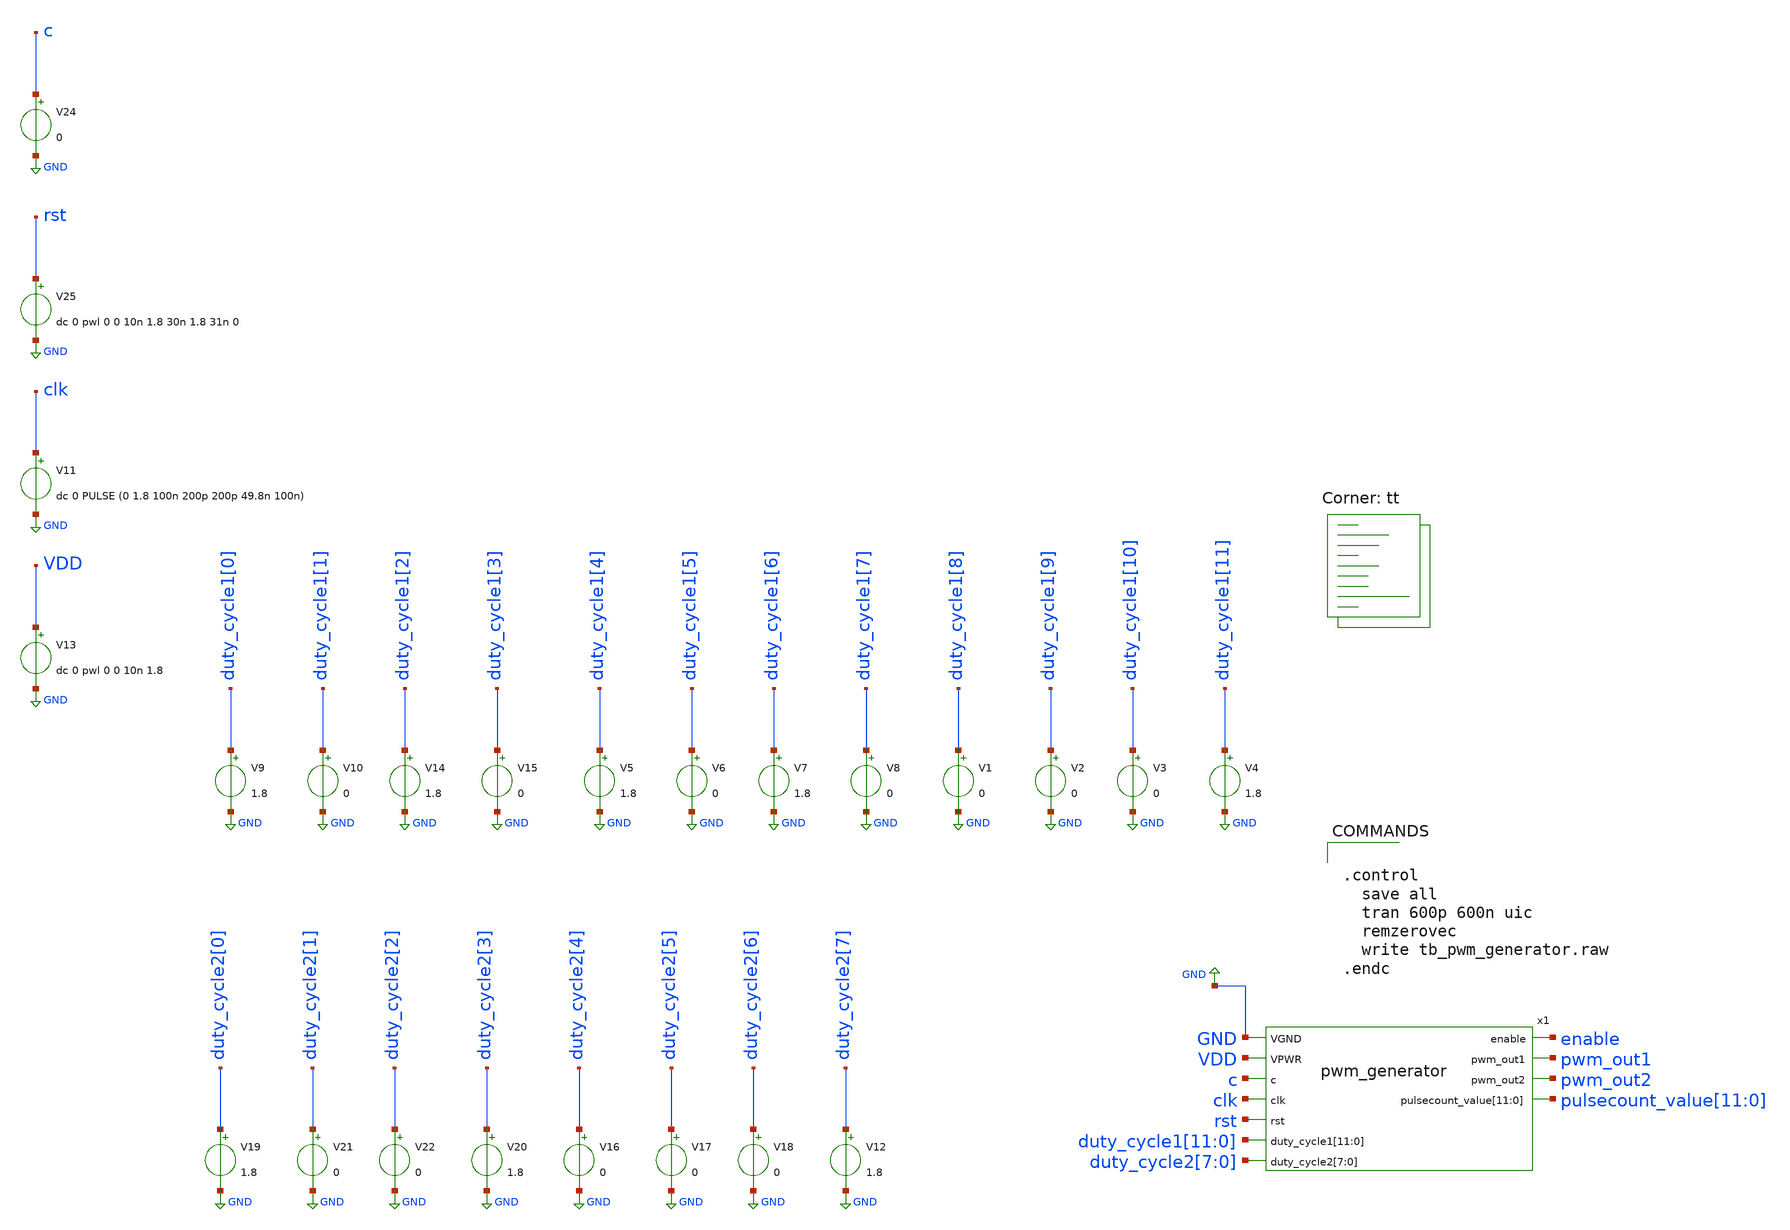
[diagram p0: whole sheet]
** sch_path: xschem/tb_pwm_generator.sch
**.subckt tb_pwm_generator
x1 enable GND pwm_out1 VDD pwm_out2 c pulsecount_value[11] pulsecount_value[10] pulsecount_value[9]
+ pulsecount_value[8] pulsecount_value[7] pulsecount_value[6] pulsecount_value[5] pulsecount_value[4] pulsecount_value[3]
+ pulsecount_value[2] pulsecount_value[1] pulsecount_value[0] clk rst duty_cycle1[11] duty_cycle1[10] duty_cycle1[9]
+ duty_cycle1[8] duty_cycle1[7] duty_cycle1[6] duty_cycle1[5] duty_cycle1[4] duty_cycle1[3] duty_cycle1[2]
+ duty_cycle1[1] duty_cycle1[0] duty_cycle2[7] duty_cycle2[6] duty_cycle2[5] duty_cycle2[4] duty_cycle2[3]
+ duty_cycle2[2] duty_cycle2[1] duty_cycle2[0] pwm_generator
V1 duty_cycle1[8] GND 0
V2 duty_cycle1[9] GND 0
V3 duty_cycle1[10] GND 0
V4 duty_cycle1[11] GND 1.8
V5 duty_cycle1[4] GND 1.8
V6 duty_cycle1[5] GND 0
V7 duty_cycle1[6] GND 1.8
V8 duty_cycle1[7] GND 0
V9 duty_cycle1[0] GND 1.8
V10 duty_cycle1[1] GND 0
V14 duty_cycle1[2] GND 1.8
V15 duty_cycle1[3] GND 0
V16 duty_cycle2[4] GND 0
V17 duty_cycle2[5] GND 0
V18 duty_cycle2[6] GND 0
V12 duty_cycle2[7] GND 1.8
V19 duty_cycle2[0] GND 1.8
V21 duty_cycle2[1] GND 0
V22 duty_cycle2[2] GND 0
V20 duty_cycle2[3] GND 1.8
V11 clk GND dc 0 PULSE (0 1.8 100n 200p 200p 49.8n 100n)
V13 VDD GND dc 0 pwl 0 0 10n 1.8
V24 c GND 0
V25 rst GND dc 0 pwl 0 0 10n 1.8 30n 1.8 31n 0
**** begin user architecture code


.control
  save all
  tran 600p 600n uic
  remzerovec
  write tb_pwm_generator.raw
.endc



** opencircuitdesign pdks install
.include $::SKYWATER_STDCELLS/sky130_fd_sc_hd.spice


.lib $::SKYWATER_MODELS/sky130.lib.spice tt
**** end user architecture code
**.ends

* expanding   symbol:  pwm_generator.sym # of pins=11
** sym_path: xschem/pwm_generator.sym
** sch_path: xschem/pwm_generator.sch
.subckt pwm_generator enable VGND pwm_out1 VPWR pwm_out2 c pulsecount_value[11] pulsecount_value[10]
+ pulsecount_value[9] pulsecount_value[8] pulsecount_value[7] pulsecount_value[6] pulsecount_value[5] pulsecount_value[4]
+ pulsecount_value[3] pulsecount_value[2] pulsecount_value[1] pulsecount_value[0] clk rst duty_cycle1[11] duty_cycle1[10]
+ duty_cycle1[9] duty_cycle1[8] duty_cycle1[7] duty_cycle1[6] duty_cycle1[5] duty_cycle1[4] duty_cycle1[3]
+ duty_cycle1[2] duty_cycle1[1] duty_cycle1[0] duty_cycle2[7] duty_cycle2[6] duty_cycle2[5] duty_cycle2[4]
+ duty_cycle2[3] duty_cycle2[2] duty_cycle2[1] duty_cycle2[0]
*.ipin VGND
*.ipin VPWR
*.ipin c
*.ipin clk
*.opin enable
*.opin pwm_out1
*.opin pwm_out2
*.ipin rst
*.ipin
*+ duty_cycle1[11],duty_cycle1[10],duty_cycle1[9],duty_cycle1[8],duty_cycle1[7],duty_cycle1[6],duty_cycle1[5],duty_cycle1[4],duty_cycle1[3],duty_cycle1[2],duty_cycle1[1],duty_cycle1[0]
*.ipin
*+ duty_cycle2[7],duty_cycle2[6],duty_cycle2[5],duty_cycle2[4],duty_cycle2[3],duty_cycle2[2],duty_cycle2[1],duty_cycle2[0]
*.opin
*+ pulsecount_value[11],pulsecount_value[10],pulsecount_value[9],pulsecount_value[8],pulsecount_value[7],pulsecount_value[6],pulsecount_value[5],pulsecount_value[4],pulsecount_value[3],pulsecount_value[2],pulsecount_value[1],pulsecount_value[0]
X_274_ prev_pwm_out1 net36 pulse__counter_o0_c pulse__counter_o1_c VGND VGND VPWR VPWR _084_
+ sky130_fd_sc_hd__and4b_1
X_275_ pulse__counter_o3_c pulse__counter_o2_c _084_ VGND VGND VPWR VPWR _085_
+ sky130_fd_sc_hd__and3_1
X_276_ pulse__counter_o5_c pulse__counter_o4_c _085_ VGND VGND VPWR VPWR _086_
+ sky130_fd_sc_hd__and3_1
X_277_ pulse__counter_o8_c pulse__counter_o7_c pulse__counter_o6_c _086_ VGND VGND VPWR VPWR _087_
+ sky130_fd_sc_hd__and4_1
X_278_ pulse__counter_o10_c pulse__counter_o9_c _087_ VGND VGND VPWR VPWR _088_
+ sky130_fd_sc_hd__and3_1
X_279_ net39 _088_ VGND VGND VPWR VPWR _083_ sky130_fd_sc_hd__xor2_1
X_280_ net67 _087_ net52 VGND VGND VPWR VPWR _089_ sky130_fd_sc_hd__a21oi_1
X_281_ _088_ _089_ VGND VGND VPWR VPWR _082_ sky130_fd_sc_hd__nor2_1
X_282_ net54 _087_ VGND VGND VPWR VPWR _081_ sky130_fd_sc_hd__xor2_1
X_283_ pulse__counter_o7_c pulse__counter_o6_c _086_ pulse__counter_o8_c VGND VGND VPWR VPWR _090_
+ sky130_fd_sc_hd__a31o_1
X_284_ _087_ _090_ VGND VGND VPWR VPWR _091_ sky130_fd_sc_hd__and2b_1
X_285_ _091_ VGND VGND VPWR VPWR _080_ sky130_fd_sc_hd__clkbuf_1
X_286_ pulse__counter_o6_c _086_ VGND VGND VPWR VPWR _092_ sky130_fd_sc_hd__nand2_1
X_287_ net49 _092_ VGND VGND VPWR VPWR _079_ sky130_fd_sc_hd__xnor2_1
X_288_ pulse__counter_o6_c _086_ VGND VGND VPWR VPWR _093_ sky130_fd_sc_hd__or2_1
X_289_ _092_ _093_ VGND VGND VPWR VPWR _094_ sky130_fd_sc_hd__and2_1
X_290_ _094_ VGND VGND VPWR VPWR _078_ sky130_fd_sc_hd__clkbuf_1
X_291_ pulse__counter_o4_c _085_ pulse__counter_o5_c VGND VGND VPWR VPWR _095_
+ sky130_fd_sc_hd__a21o_1
X_292_ _086_ _095_ VGND VGND VPWR VPWR _096_ sky130_fd_sc_hd__and2b_1
X_293_ _096_ VGND VGND VPWR VPWR _077_ sky130_fd_sc_hd__clkbuf_1
X_294_ net41 _085_ VGND VGND VPWR VPWR _076_ sky130_fd_sc_hd__xor2_1
X_295_ net66 _084_ net42 VGND VGND VPWR VPWR _097_ sky130_fd_sc_hd__a21oi_1
X_296_ _085_ _097_ VGND VGND VPWR VPWR _075_ sky130_fd_sc_hd__nor2_1
X_297_ net47 _084_ VGND VGND VPWR VPWR _074_ sky130_fd_sc_hd__xor2_1
X_298_ prev_pwm_out1 VGND VGND VPWR VPWR _098_ sky130_fd_sc_hd__inv_2
X_299_ pulse__counter_o0_c net36 _098_ VGND VGND VPWR VPWR _099_ sky130_fd_sc_hd__and3_1
X_300_ net59 _099_ _084_ VGND VGND VPWR VPWR _073_ sky130_fd_sc_hd__o21ba_1
X_301_ net36 _098_ net61 VGND VGND VPWR VPWR _100_ sky130_fd_sc_hd__a21oi_1
X_302_ _099_ net62 VGND VGND VPWR VPWR _072_ sky130_fd_sc_hd__nor2_1
X_303_ net20 VGND VGND VPWR VPWR _101_ sky130_fd_sc_hd__inv_2
X_304_ counter2_o7_c _101_ VGND VGND VPWR VPWR _102_ sky130_fd_sc_hd__nand2_1
X_305_ counter2_o6_c VGND VGND VPWR VPWR _103_ sky130_fd_sc_hd__inv_2
X_306_ counter2_o3_c VGND VGND VPWR VPWR _104_ sky130_fd_sc_hd__inv_2
X_307_ net15 counter2_o2_c VGND VGND VPWR VPWR _105_ sky130_fd_sc_hd__or2b_1
X_308_ counter2_o1_c net14 VGND VGND VPWR VPWR _106_ sky130_fd_sc_hd__and2b_1
X_309_ counter2_o2_c net15 VGND VGND VPWR VPWR _107_ sky130_fd_sc_hd__and2b_1
X_310_ _104_ net16 _105_ _106_ _107_ VGND VGND VPWR VPWR _108_ sky130_fd_sc_hd__a221o_1
X_311_ counter2_o4_c VGND VGND VPWR VPWR _109_ sky130_fd_sc_hd__inv_2
X_312_ _109_ net17 net16 _104_ VGND VGND VPWR VPWR _110_ sky130_fd_sc_hd__o22a_1
X_313_ counter2_o5_c VGND VGND VPWR VPWR _111_ sky130_fd_sc_hd__inv_2
X_314_ _109_ net17 net18 _111_ VGND VGND VPWR VPWR _112_ sky130_fd_sc_hd__a22o_1
X_315_ _108_ _110_ _112_ VGND VGND VPWR VPWR _113_ sky130_fd_sc_hd__a21o_1
X_316_ _103_ net19 net18 _111_ VGND VGND VPWR VPWR _114_ sky130_fd_sc_hd__o22a_1
X_317_ _103_ net19 _113_ _114_ VGND VGND VPWR VPWR _115_ sky130_fd_sc_hd__a22o_1
X_318_ counter2_o7_c _101_ VGND VGND VPWR VPWR _116_ sky130_fd_sc_hd__nor2_1
X_319_ _102_ _115_ _116_ net21 VGND VGND VPWR VPWR _117_ sky130_fd_sc_hd__a211o_2
X_320_ counter2_o3_c counter2_o2_c counter2_o1_c counter2_o0_c VGND VGND VPWR VPWR _118_
+ sky130_fd_sc_hd__and4_1
X_321_ counter2_o4_c _118_ VGND VGND VPWR VPWR _119_ sky130_fd_sc_hd__nand2_1
X_322_ _111_ _119_ VGND VGND VPWR VPWR _120_ sky130_fd_sc_hd__nor2_1
X_323_ counter2_o6_c _120_ VGND VGND VPWR VPWR _121_ sky130_fd_sc_hd__nand2_1
X_324_ counter2_o7_c _121_ VGND VGND VPWR VPWR _122_ sky130_fd_sc_hd__xnor2_1
X_325_ _117_ _122_ VGND VGND VPWR VPWR _123_ sky130_fd_sc_hd__and2_1
X_326_ _123_ VGND VGND VPWR VPWR _071_ sky130_fd_sc_hd__clkbuf_1
X_327_ counter2_o6_c _120_ VGND VGND VPWR VPWR _124_ sky130_fd_sc_hd__or2_1
X_328_ _117_ _121_ _124_ VGND VGND VPWR VPWR _125_ sky130_fd_sc_hd__and3_1
X_329_ _125_ VGND VGND VPWR VPWR _070_ sky130_fd_sc_hd__clkbuf_1
X_330_ _120_ VGND VGND VPWR VPWR _126_ sky130_fd_sc_hd__inv_2
X_331_ _111_ _119_ VGND VGND VPWR VPWR _127_ sky130_fd_sc_hd__nand2_1
X_332_ _117_ _126_ _127_ VGND VGND VPWR VPWR _128_ sky130_fd_sc_hd__and3_1
X_333_ _128_ VGND VGND VPWR VPWR _069_ sky130_fd_sc_hd__clkbuf_1
X_334_ counter2_o4_c _118_ VGND VGND VPWR VPWR _129_ sky130_fd_sc_hd__or2_1
X_335_ _117_ _119_ _129_ VGND VGND VPWR VPWR _130_ sky130_fd_sc_hd__and3_1
X_336_ _130_ VGND VGND VPWR VPWR _068_ sky130_fd_sc_hd__clkbuf_1
X_337_ _118_ VGND VGND VPWR VPWR _131_ sky130_fd_sc_hd__inv_2
X_338_ counter2_o2_c counter2_o1_c counter2_o0_c VGND VGND VPWR VPWR _132_ sky130_fd_sc_hd__nand3_1
X_339_ _104_ _132_ VGND VGND VPWR VPWR _133_ sky130_fd_sc_hd__nand2_1
X_340_ _117_ _131_ _133_ VGND VGND VPWR VPWR _134_ sky130_fd_sc_hd__and3_1
X_341_ _134_ VGND VGND VPWR VPWR _067_ sky130_fd_sc_hd__clkbuf_1
X_342_ counter2_o1_c counter2_o0_c counter2_o2_c VGND VGND VPWR VPWR _135_ sky130_fd_sc_hd__a21o_1
X_343_ _117_ _132_ _135_ VGND VGND VPWR VPWR _136_ sky130_fd_sc_hd__and3_1
X_344_ _136_ VGND VGND VPWR VPWR _066_ sky130_fd_sc_hd__clkbuf_1
X_345_ counter2_o1_c counter2_o0_c VGND VGND VPWR VPWR _137_ sky130_fd_sc_hd__nand2_1
X_346_ counter2_o1_c counter2_o0_c VGND VGND VPWR VPWR _138_ sky130_fd_sc_hd__or2_1
X_347_ _117_ _137_ _138_ VGND VGND VPWR VPWR _139_ sky130_fd_sc_hd__and3_1
X_348_ _139_ VGND VGND VPWR VPWR _065_ sky130_fd_sc_hd__clkbuf_1
X_349_ counter2_o0_c _117_ VGND VGND VPWR VPWR _140_ sky130_fd_sc_hd__and2b_1
X_350_ _140_ VGND VGND VPWR VPWR _064_ sky130_fd_sc_hd__clkbuf_1
X_351_ counter1_o11_c VGND VGND VPWR VPWR _141_ sky130_fd_sc_hd__inv_2
X_352_ _141_ net3 net4 VGND VGND VPWR VPWR _142_ sky130_fd_sc_hd__a21oi_2
X_353_ _142_ VGND VGND VPWR VPWR _143_ sky130_fd_sc_hd__buf_2
X_354_ net13 VGND VGND VPWR VPWR _144_ sky130_fd_sc_hd__inv_2
X_355_ counter1_o10_c _144_ VGND VGND VPWR VPWR _145_ sky130_fd_sc_hd__or2_1
X_356_ counter1_o9_c net12 VGND VGND VPWR VPWR _146_ sky130_fd_sc_hd__xnor2_1
X_357_ net11 counter1_o8_c VGND VGND VPWR VPWR _147_ sky130_fd_sc_hd__or2b_1
X_358_ net10 counter1_o7_c VGND VGND VPWR VPWR _148_ sky130_fd_sc_hd__or2b_1
X_359_ _147_ _148_ VGND VGND VPWR VPWR _149_ sky130_fd_sc_hd__nand2_1
X_360_ counter1_o8_c net11 VGND VGND VPWR VPWR _150_ sky130_fd_sc_hd__or2b_1
X_361_ net9 VGND VGND VPWR VPWR _151_ sky130_fd_sc_hd__inv_2
X_362_ net8 VGND VGND VPWR VPWR _152_ sky130_fd_sc_hd__inv_2
X_363_ counter1_o6_c _151_ _152_ counter1_o5_c VGND VGND VPWR VPWR _153_ sky130_fd_sc_hd__a22o_1
X_364_ counter1_o4_c VGND VGND VPWR VPWR _154_ sky130_fd_sc_hd__inv_2
X_365_ _154_ net7 VGND VGND VPWR VPWR _155_ sky130_fd_sc_hd__nand2_1
X_366_ counter1_o7_c net10 VGND VGND VPWR VPWR _156_ sky130_fd_sc_hd__or2b_1
X_367_ _147_ _148_ _156_ _150_ VGND VGND VPWR VPWR _157_ sky130_fd_sc_hd__and4_1
X_368_ counter1_o6_c _151_ _152_ counter1_o5_c VGND VGND VPWR VPWR _158_ sky130_fd_sc_hd__o22a_1
X_369_ _153_ _155_ _157_ _158_ VGND VGND VPWR VPWR _159_ sky130_fd_sc_hd__and4b_1
X_370_ net6 VGND VGND VPWR VPWR _160_ sky130_fd_sc_hd__inv_2
X_371_ net5 VGND VGND VPWR VPWR _161_ sky130_fd_sc_hd__inv_2
X_372_ net2 VGND VGND VPWR VPWR _162_ sky130_fd_sc_hd__inv_2
X_373_ counter1_o2_c _161_ _162_ counter1_o1_c VGND VGND VPWR VPWR _163_ sky130_fd_sc_hd__a211o_1
X_374_ counter1_o2_c _161_ _160_ counter1_o3_c VGND VGND VPWR VPWR _164_ sky130_fd_sc_hd__o22a_1
X_375_ _154_ net7 VGND VGND VPWR VPWR _165_ sky130_fd_sc_hd__nor2_1
X_376_ counter1_o3_c _160_ _163_ _164_ _165_ VGND VGND VPWR VPWR _166_ sky130_fd_sc_hd__a221o_1
X_377_ counter1_o6_c _151_ _153_ _157_ VGND VGND VPWR VPWR _167_ sky130_fd_sc_hd__o211a_1
X_378_ _149_ _150_ _159_ _166_ _167_ VGND VGND VPWR VPWR _168_ sky130_fd_sc_hd__a221o_1
X_379_ net3 VGND VGND VPWR VPWR _169_ sky130_fd_sc_hd__inv_2
X_380_ net12 _145_ counter1_o9_c VGND VGND VPWR VPWR _170_ sky130_fd_sc_hd__and3b_1
X_381_ counter1_o11_c _169_ _144_ counter1_o10_c _170_ VGND VGND VPWR VPWR _171_
+ sky130_fd_sc_hd__a221o_1
X_382_ _145_ _146_ _168_ _171_ VGND VGND VPWR VPWR _172_ sky130_fd_sc_hd__a31o_1
X_383_ _172_ VGND VGND VPWR VPWR _173_ sky130_fd_sc_hd__buf_2
X_384_ counter1_o3_c counter1_o2_c counter1_o1_c counter1_o0_c VGND VGND VPWR VPWR _174_
+ sky130_fd_sc_hd__and4_1
X_385_ _174_ VGND VGND VPWR VPWR _175_ sky130_fd_sc_hd__dlymetal6s2s_1
X_386_ counter1_o5_c counter1_o4_c VGND VGND VPWR VPWR _176_ sky130_fd_sc_hd__and2_1
X_387_ counter1_o7_c counter1_o6_c _175_ _176_ VGND VGND VPWR VPWR _177_ sky130_fd_sc_hd__and4_1
X_388_ counter1_o9_c counter1_o8_c _177_ VGND VGND VPWR VPWR _178_ sky130_fd_sc_hd__and3_1
X_389_ counter1_o10_c _178_ VGND VGND VPWR VPWR _179_ sky130_fd_sc_hd__and2_1
X_390_ net64 _179_ VGND VGND VPWR VPWR _180_ sky130_fd_sc_hd__xnor2_1
X_391_ _143_ _173_ _180_ VGND VGND VPWR VPWR _063_ sky130_fd_sc_hd__a21oi_1
X_392_ counter1_o10_c _178_ VGND VGND VPWR VPWR _181_ sky130_fd_sc_hd__nor2_1
X_393_ _143_ _173_ _179_ _181_ VGND VGND VPWR VPWR _062_ sky130_fd_sc_hd__a211oi_1
X_394_ counter1_o8_c _177_ counter1_o9_c VGND VGND VPWR VPWR _182_ sky130_fd_sc_hd__a21oi_1
X_395_ _143_ _173_ _178_ _182_ VGND VGND VPWR VPWR _061_ sky130_fd_sc_hd__a211oi_1
X_396_ counter1_o8_c _177_ VGND VGND VPWR VPWR _183_ sky130_fd_sc_hd__xnor2_1
X_397_ _143_ _173_ _183_ VGND VGND VPWR VPWR _060_ sky130_fd_sc_hd__a21oi_1
X_398_ _175_ _176_ VGND VGND VPWR VPWR _184_ sky130_fd_sc_hd__and2_1
X_399_ counter1_o6_c _184_ counter1_o7_c VGND VGND VPWR VPWR _185_ sky130_fd_sc_hd__a21oi_1
X_400_ _143_ _173_ _177_ _185_ VGND VGND VPWR VPWR _059_ sky130_fd_sc_hd__a211oi_1
X_401_ counter1_o6_c _184_ VGND VGND VPWR VPWR _186_ sky130_fd_sc_hd__xnor2_1
X_402_ _143_ _173_ _186_ VGND VGND VPWR VPWR _058_ sky130_fd_sc_hd__a21oi_1
X_403_ counter1_o4_c _175_ counter1_o5_c VGND VGND VPWR VPWR _187_ sky130_fd_sc_hd__a21oi_1
X_404_ _142_ _172_ _184_ _187_ VGND VGND VPWR VPWR _057_ sky130_fd_sc_hd__a211oi_1
X_405_ counter1_o4_c _175_ VGND VGND VPWR VPWR _188_ sky130_fd_sc_hd__xnor2_1
X_406_ _143_ _173_ _188_ VGND VGND VPWR VPWR _056_ sky130_fd_sc_hd__a21oi_1
X_407_ counter1_o2_c counter1_o1_c counter1_o0_c VGND VGND VPWR VPWR _189_ sky130_fd_sc_hd__and3_1
X_408_ counter1_o3_c _189_ VGND VGND VPWR VPWR _190_ sky130_fd_sc_hd__nor2_1
X_409_ _142_ _172_ _175_ _190_ VGND VGND VPWR VPWR _055_ sky130_fd_sc_hd__a211oi_1
X_410_ counter1_o1_c counter1_o0_c counter1_o2_c VGND VGND VPWR VPWR _191_ sky130_fd_sc_hd__a21oi_1
X_411_ _142_ _172_ _189_ _191_ VGND VGND VPWR VPWR _054_ sky130_fd_sc_hd__a211oi_1
X_412_ net65 net40 VGND VGND VPWR VPWR _192_ sky130_fd_sc_hd__xnor2_1
X_413_ _143_ _173_ _192_ VGND VGND VPWR VPWR _053_ sky130_fd_sc_hd__a21oi_1
X_414_ _143_ _173_ net40 VGND VGND VPWR VPWR _052_ sky130_fd_sc_hd__a21oi_1
X_415_ pulse__counter_o11_c pulse__counter_o10_c pulse__counter_o9_c pulse__counter_o8_c VGND VGND
+ VPWR VPWR _193_ sky130_fd_sc_hd__nor4_1
X_416_ pulse__counter_o3_c pulse__counter_o2_c pulse__counter_o1_c pulse__counter_o0_c VGND VGND
+ VPWR VPWR _194_ sky130_fd_sc_hd__and4b_1
X_417_ pulse__counter_o7_c pulse__counter_o6_c pulse__counter_o5_c pulse__counter_o4_c VGND VGND
+ VPWR VPWR _195_ sky130_fd_sc_hd__nor4_1
X_418_ _193_ _194_ _195_ net38 VGND VGND VPWR VPWR _039_ sky130_fd_sc_hd__a31o_1
X_419_ net21 counter2_o7_c VGND VGND VPWR VPWR _196_ sky130_fd_sc_hd__and2b_1
X_420_ _109_ net18 VGND VGND VPWR VPWR _197_ sky130_fd_sc_hd__or2_1
X_421_ counter2_o0_c net14 VGND VGND VPWR VPWR _198_ sky130_fd_sc_hd__and2b_1
X_422_ counter2_o1_c net15 VGND VGND VPWR VPWR _199_ sky130_fd_sc_hd__and2b_1
X_423_ net15 counter2_o1_c VGND VGND VPWR VPWR _200_ sky130_fd_sc_hd__and2b_1
X_424_ net14 counter2_o0_c VGND VGND VPWR VPWR _201_ sky130_fd_sc_hd__and2b_1
X_425_ _199_ _200_ _201_ VGND VGND VPWR VPWR _202_ sky130_fd_sc_hd__or3_1
X_426_ counter2_o3_c net17 VGND VGND VPWR VPWR _203_ sky130_fd_sc_hd__or2b_1
X_427_ net17 counter2_o3_c VGND VGND VPWR VPWR _204_ sky130_fd_sc_hd__or2b_1
X_428_ counter2_o2_c net16 VGND VGND VPWR VPWR _205_ sky130_fd_sc_hd__or2b_1
X_429_ net16 counter2_o2_c VGND VGND VPWR VPWR _206_ sky130_fd_sc_hd__or2b_1
X_430_ _203_ _204_ _205_ _206_ VGND VGND VPWR VPWR _207_ sky130_fd_sc_hd__and4_1
X_431_ _198_ _202_ _207_ VGND VGND VPWR VPWR _208_ sky130_fd_sc_hd__or3b_1
X_432_ _200_ _201_ _199_ VGND VGND VPWR VPWR _209_ sky130_fd_sc_hd__o21bai_1
X_433_ counter2_o2_c net16 _204_ VGND VGND VPWR VPWR _210_ sky130_fd_sc_hd__and3b_1
X_434_ _104_ net17 _207_ _209_ _210_ VGND VGND VPWR VPWR _211_ sky130_fd_sc_hd__a221o_1
X_435_ _111_ net19 net18 _109_ VGND VGND VPWR VPWR _212_ sky130_fd_sc_hd__a22o_1
X_436_ _197_ _208_ _211_ _212_ VGND VGND VPWR VPWR _213_ sky130_fd_sc_hd__a31oi_1
X_437_ net19 _111_ counter2_o6_c _101_ VGND VGND VPWR VPWR _214_ sky130_fd_sc_hd__a2bb2o_1
X_438_ counter2_o7_c net21 VGND VGND VPWR VPWR _215_ sky130_fd_sc_hd__or2b_1
X_439_ counter2_o6_c _101_ _213_ _214_ _215_ VGND VGND VPWR VPWR _216_ sky130_fd_sc_hd__o221a_1
X_440_ _196_ _216_ _117_ VGND VGND VPWR VPWR _038_ sky130_fd_sc_hd__o21ai_1
X_441_ counter1_o8_c VGND VGND VPWR VPWR _217_ sky130_fd_sc_hd__inv_2
X_442_ _141_ net4 _169_ counter1_o10_c VGND VGND VPWR VPWR _218_ sky130_fd_sc_hd__a22o_1
X_443_ _141_ net4 VGND VGND VPWR VPWR _219_ sky130_fd_sc_hd__or2_1
X_444_ counter1_o9_c VGND VGND VPWR VPWR _220_ sky130_fd_sc_hd__inv_2
X_445_ counter1_o10_c _169_ net13 _220_ VGND VGND VPWR VPWR _221_ sky130_fd_sc_hd__o22a_1
X_446_ _218_ _219_ _221_ VGND VGND VPWR VPWR _222_ sky130_fd_sc_hd__and3b_1
X_447_ _220_ net13 net12 _217_ VGND VGND VPWR VPWR _223_ sky130_fd_sc_hd__a22o_1
X_448_ _223_ VGND VGND VPWR VPWR _224_ sky130_fd_sc_hd__inv_2
X_449_ _217_ net12 _222_ _224_ VGND VGND VPWR VPWR _225_ sky130_fd_sc_hd__o211a_1
X_450_ net5 counter1_o1_c VGND VGND VPWR VPWR _226_ sky130_fd_sc_hd__or2b_1
X_451_ net2 counter1_o0_c VGND VGND VPWR VPWR _227_ sky130_fd_sc_hd__or2b_1
X_452_ counter1_o1_c net5 VGND VGND VPWR VPWR _228_ sky130_fd_sc_hd__and2b_1
X_453_ _226_ _227_ _228_ VGND VGND VPWR VPWR _229_ sky130_fd_sc_hd__a21o_1
X_454_ counter1_o2_c net6 VGND VGND VPWR VPWR _230_ sky130_fd_sc_hd__or2b_1
X_455_ counter1_o3_c net7 VGND VGND VPWR VPWR _231_ sky130_fd_sc_hd__or2b_1
X_456_ net7 counter1_o3_c VGND VGND VPWR VPWR _232_ sky130_fd_sc_hd__or2b_1
X_457_ net6 counter1_o2_c VGND VGND VPWR VPWR _233_ sky130_fd_sc_hd__or2b_1
X_458_ _230_ _231_ _232_ _233_ VGND VGND VPWR VPWR _234_ sky130_fd_sc_hd__and4_1
X_459_ _230_ _231_ _232_ VGND VGND VPWR VPWR _235_ sky130_fd_sc_hd__a21boi_1
X_460_ _229_ _234_ _235_ VGND VGND VPWR VPWR _236_ sky130_fd_sc_hd__a21o_1
X_461_ _154_ net8 VGND VGND VPWR VPWR _237_ sky130_fd_sc_hd__nor2_1
X_462_ counter1_o5_c VGND VGND VPWR VPWR _238_ sky130_fd_sc_hd__inv_2
X_463_ _238_ net9 net8 _154_ VGND VGND VPWR VPWR _239_ sky130_fd_sc_hd__a22o_1
X_464_ counter1_o6_c VGND VGND VPWR VPWR _240_ sky130_fd_sc_hd__inv_2
X_465_ net11 counter1_o7_c VGND VGND VPWR VPWR _241_ sky130_fd_sc_hd__or2b_1
X_466_ _240_ net10 net9 _238_ _241_ VGND VGND VPWR VPWR _242_ sky130_fd_sc_hd__o221a_1
X_467_ net11 VGND VGND VPWR VPWR _243_ sky130_fd_sc_hd__inv_2
X_468_ net10 _240_ counter1_o7_c _243_ VGND VGND VPWR VPWR _244_ sky130_fd_sc_hd__o2bb2a_1
X_469_ _237_ _239_ _242_ _244_ VGND VGND VPWR VPWR _245_ sky130_fd_sc_hd__and4bb_1
X_470_ _244_ _241_ VGND VGND VPWR VPWR _246_ sky130_fd_sc_hd__and2b_1
X_471_ _244_ _242_ _239_ VGND VGND VPWR VPWR _247_ sky130_fd_sc_hd__and3_1
X_472_ _236_ _245_ _246_ _247_ VGND VGND VPWR VPWR _248_ sky130_fd_sc_hd__a211o_1
X_473_ counter1_o10_c net3 _219_ VGND VGND VPWR VPWR _249_ sky130_fd_sc_hd__and3b_1
X_474_ _141_ net4 _222_ _223_ _249_ VGND VGND VPWR VPWR _250_ sky130_fd_sc_hd__a221o_1
X_475_ _225_ _248_ _250_ VGND VGND VPWR VPWR _251_ sky130_fd_sc_hd__a21o_1
X_476_ _228_ _227_ VGND VGND VPWR VPWR _252_ sky130_fd_sc_hd__and2b_1
X_477_ counter1_o0_c _162_ _226_ _252_ VGND VGND VPWR VPWR _253_ sky130_fd_sc_hd__o211a_1
X_478_ _225_ _234_ _245_ _253_ VGND VGND VPWR VPWR _254_ sky130_fd_sc_hd__nand4_1
X_479_ _143_ _173_ _251_ _254_ VGND VGND VPWR VPWR _037_ sky130_fd_sc_hd__a22o_1
X_480_ net36 VGND VGND VPWR VPWR _255_ sky130_fd_sc_hd__clkbuf_1
X_481_ _255_ VGND VGND VPWR VPWR _036_ sky130_fd_sc_hd__clkbuf_1
X_482_ net22 VGND VGND VPWR VPWR _256_ sky130_fd_sc_hd__clkbuf_4
X_483_ _256_ VGND VGND VPWR VPWR _000_ sky130_fd_sc_hd__inv_2
X_484_ _256_ VGND VGND VPWR VPWR _257_ sky130_fd_sc_hd__buf_4
X_485_ _257_ VGND VGND VPWR VPWR _001_ sky130_fd_sc_hd__inv_2
X_486_ _257_ VGND VGND VPWR VPWR _002_ sky130_fd_sc_hd__inv_2
X_487_ _257_ VGND VGND VPWR VPWR _003_ sky130_fd_sc_hd__inv_2
X_488_ net1 _000_ VGND VGND VPWR VPWR _258_ sky130_fd_sc_hd__nand2_1
X_489_ _258_ VGND VGND VPWR VPWR _259_ sky130_fd_sc_hd__clkbuf_4
X_490_ pulse__counter_o0_c net63 _259_ VGND VGND VPWR VPWR _260_ sky130_fd_sc_hd__mux2_1
X_491_ _260_ VGND VGND VPWR VPWR _040_ sky130_fd_sc_hd__clkbuf_1
X_492_ pulse__counter_o1_c net60 _259_ VGND VGND VPWR VPWR _261_ sky130_fd_sc_hd__mux2_1
X_493_ _261_ VGND VGND VPWR VPWR _041_ sky130_fd_sc_hd__clkbuf_1
X_494_ pulse__counter_o2_c net53 _259_ VGND VGND VPWR VPWR _262_ sky130_fd_sc_hd__mux2_1
X_495_ _262_ VGND VGND VPWR VPWR _042_ sky130_fd_sc_hd__clkbuf_1
X_496_ pulse__counter_o3_c net50 _259_ VGND VGND VPWR VPWR _263_ sky130_fd_sc_hd__mux2_1
X_497_ _263_ VGND VGND VPWR VPWR _043_ sky130_fd_sc_hd__clkbuf_1
X_498_ pulse__counter_o4_c net48 _259_ VGND VGND VPWR VPWR _264_ sky130_fd_sc_hd__mux2_1
X_499_ _264_ VGND VGND VPWR VPWR _044_ sky130_fd_sc_hd__clkbuf_1
X_500_ pulse__counter_o5_c net45 _259_ VGND VGND VPWR VPWR _265_ sky130_fd_sc_hd__mux2_1
X_501_ _265_ VGND VGND VPWR VPWR _045_ sky130_fd_sc_hd__clkbuf_1
X_502_ pulse__counter_o6_c net51 _259_ VGND VGND VPWR VPWR _266_ sky130_fd_sc_hd__mux2_1
X_503_ _266_ VGND VGND VPWR VPWR _046_ sky130_fd_sc_hd__clkbuf_1
X_504_ pulse__counter_o7_c net44 _259_ VGND VGND VPWR VPWR _267_ sky130_fd_sc_hd__mux2_1
X_505_ _267_ VGND VGND VPWR VPWR _047_ sky130_fd_sc_hd__clkbuf_1
X_506_ pulse__counter_o8_c net43 _259_ VGND VGND VPWR VPWR _268_ sky130_fd_sc_hd__mux2_1
X_507_ _268_ VGND VGND VPWR VPWR _048_ sky130_fd_sc_hd__clkbuf_1
X_508_ pulse__counter_o9_c net46 _259_ VGND VGND VPWR VPWR _269_ sky130_fd_sc_hd__mux2_1
X_509_ _269_ VGND VGND VPWR VPWR _049_ sky130_fd_sc_hd__clkbuf_1
X_510_ pulse__counter_o10_c net55 _258_ VGND VGND VPWR VPWR _270_ sky130_fd_sc_hd__mux2_1
X_511_ net56 VGND VGND VPWR VPWR _050_ sky130_fd_sc_hd__clkbuf_1
X_512_ pulse__counter_o11_c net57 _258_ VGND VGND VPWR VPWR _271_ sky130_fd_sc_hd__mux2_1
X_513_ net58 VGND VGND VPWR VPWR _051_ sky130_fd_sc_hd__clkbuf_1
X_514_ _257_ VGND VGND VPWR VPWR _004_ sky130_fd_sc_hd__inv_2
X_515_ _257_ VGND VGND VPWR VPWR _005_ sky130_fd_sc_hd__inv_2
X_516_ _257_ VGND VGND VPWR VPWR _006_ sky130_fd_sc_hd__inv_2
X_517_ _257_ VGND VGND VPWR VPWR _007_ sky130_fd_sc_hd__inv_2
X_518_ _257_ VGND VGND VPWR VPWR _008_ sky130_fd_sc_hd__inv_2
X_519_ _257_ VGND VGND VPWR VPWR _009_ sky130_fd_sc_hd__inv_2
X_520_ _257_ VGND VGND VPWR VPWR _010_ sky130_fd_sc_hd__inv_2
X_521_ _256_ VGND VGND VPWR VPWR _272_ sky130_fd_sc_hd__buf_4
X_522_ _272_ VGND VGND VPWR VPWR _011_ sky130_fd_sc_hd__inv_2
X_523_ _272_ VGND VGND VPWR VPWR _012_ sky130_fd_sc_hd__inv_2
X_524_ _272_ VGND VGND VPWR VPWR _013_ sky130_fd_sc_hd__inv_2
X_525_ _272_ VGND VGND VPWR VPWR _014_ sky130_fd_sc_hd__inv_2
X_526_ _272_ VGND VGND VPWR VPWR _015_ sky130_fd_sc_hd__inv_2
X_527_ _272_ VGND VGND VPWR VPWR _016_ sky130_fd_sc_hd__inv_2
X_528_ _272_ VGND VGND VPWR VPWR _017_ sky130_fd_sc_hd__inv_2
X_529_ _272_ VGND VGND VPWR VPWR _018_ sky130_fd_sc_hd__inv_2
X_530_ _272_ VGND VGND VPWR VPWR _019_ sky130_fd_sc_hd__inv_2
X_531_ _272_ VGND VGND VPWR VPWR _020_ sky130_fd_sc_hd__inv_2
X_532_ _256_ VGND VGND VPWR VPWR _273_ sky130_fd_sc_hd__buf_4
X_533_ _273_ VGND VGND VPWR VPWR _021_ sky130_fd_sc_hd__inv_2
X_534_ _273_ VGND VGND VPWR VPWR _022_ sky130_fd_sc_hd__inv_2
X_535_ _273_ VGND VGND VPWR VPWR _023_ sky130_fd_sc_hd__inv_2
X_536_ _273_ VGND VGND VPWR VPWR _024_ sky130_fd_sc_hd__inv_2
X_537_ _273_ VGND VGND VPWR VPWR _025_ sky130_fd_sc_hd__inv_2
X_538_ _273_ VGND VGND VPWR VPWR _026_ sky130_fd_sc_hd__inv_2
X_539_ _273_ VGND VGND VPWR VPWR _027_ sky130_fd_sc_hd__inv_2
X_540_ _273_ VGND VGND VPWR VPWR _028_ sky130_fd_sc_hd__inv_2
X_541_ _273_ VGND VGND VPWR VPWR _029_ sky130_fd_sc_hd__inv_2
X_542_ _273_ VGND VGND VPWR VPWR _030_ sky130_fd_sc_hd__inv_2
X_543_ _256_ VGND VGND VPWR VPWR _031_ sky130_fd_sc_hd__inv_2
X_544_ _256_ VGND VGND VPWR VPWR _032_ sky130_fd_sc_hd__inv_2
X_545_ _256_ VGND VGND VPWR VPWR _033_ sky130_fd_sc_hd__inv_2
X_546_ _256_ VGND VGND VPWR VPWR _034_ sky130_fd_sc_hd__inv_2
X_547_ _256_ VGND VGND VPWR VPWR _035_ sky130_fd_sc_hd__inv_2
X_548_ clknet_2_2__leaf_clk _036_ _000_ VGND VGND VPWR VPWR prev_pwm_out1 sky130_fd_sc_hd__dfrtp_1
X_549_ clknet_2_0__leaf_clk _037_ _001_ VGND VGND VPWR VPWR net36 sky130_fd_sc_hd__dfrtp_2
X_550_ clknet_2_2__leaf_clk _038_ _002_ VGND VGND VPWR VPWR net37 sky130_fd_sc_hd__dfrtp_1
X_551_ clknet_2_3__leaf_clk _039_ _003_ VGND VGND VPWR VPWR net23 sky130_fd_sc_hd__dfrtp_1
X_552_ clknet_2_1__leaf_clk _040_ VGND VGND VPWR VPWR net24 sky130_fd_sc_hd__dfxtp_1
X_553_ clknet_2_1__leaf_clk _041_ VGND VGND VPWR VPWR net27 sky130_fd_sc_hd__dfxtp_1
X_554_ clknet_2_1__leaf_clk _042_ VGND VGND VPWR VPWR net28 sky130_fd_sc_hd__dfxtp_1
X_555_ clknet_2_1__leaf_clk _043_ VGND VGND VPWR VPWR net29 sky130_fd_sc_hd__dfxtp_1
X_556_ clknet_2_1__leaf_clk _044_ VGND VGND VPWR VPWR net30 sky130_fd_sc_hd__dfxtp_1
X_557_ clknet_2_1__leaf_clk _045_ VGND VGND VPWR VPWR net31 sky130_fd_sc_hd__dfxtp_1
X_558_ clknet_2_3__leaf_clk _046_ VGND VGND VPWR VPWR net32 sky130_fd_sc_hd__dfxtp_1
X_559_ clknet_2_3__leaf_clk _047_ VGND VGND VPWR VPWR net33 sky130_fd_sc_hd__dfxtp_1
X_560_ clknet_2_3__leaf_clk _048_ VGND VGND VPWR VPWR net34 sky130_fd_sc_hd__dfxtp_1
X_561_ clknet_2_3__leaf_clk _049_ VGND VGND VPWR VPWR net35 sky130_fd_sc_hd__dfxtp_1
X_562_ clknet_2_3__leaf_clk _050_ VGND VGND VPWR VPWR net25 sky130_fd_sc_hd__dfxtp_1
X_563_ clknet_2_3__leaf_clk _051_ VGND VGND VPWR VPWR net26 sky130_fd_sc_hd__dfxtp_1
X_564_ clknet_2_0__leaf_clk _052_ _004_ VGND VGND VPWR VPWR counter1_o0_c sky130_fd_sc_hd__dfrtp_2
X_565_ clknet_2_0__leaf_clk _053_ _005_ VGND VGND VPWR VPWR counter1_o1_c sky130_fd_sc_hd__dfrtp_2
X_566_ clknet_2_0__leaf_clk _054_ _006_ VGND VGND VPWR VPWR counter1_o2_c sky130_fd_sc_hd__dfrtp_2
X_567_ clknet_2_0__leaf_clk _055_ _007_ VGND VGND VPWR VPWR counter1_o3_c sky130_fd_sc_hd__dfrtp_2
X_568_ clknet_2_0__leaf_clk _056_ _008_ VGND VGND VPWR VPWR counter1_o4_c sky130_fd_sc_hd__dfrtp_2
X_569_ clknet_2_0__leaf_clk _057_ _009_ VGND VGND VPWR VPWR counter1_o5_c sky130_fd_sc_hd__dfrtp_2
X_570_ clknet_2_0__leaf_clk _058_ _010_ VGND VGND VPWR VPWR counter1_o6_c sky130_fd_sc_hd__dfrtp_4
X_571_ clknet_2_0__leaf_clk _059_ _011_ VGND VGND VPWR VPWR counter1_o7_c sky130_fd_sc_hd__dfrtp_1
X_572_ clknet_2_1__leaf_clk _060_ _012_ VGND VGND VPWR VPWR counter1_o8_c sky130_fd_sc_hd__dfrtp_4
X_573_ clknet_2_1__leaf_clk _061_ _013_ VGND VGND VPWR VPWR counter1_o9_c sky130_fd_sc_hd__dfrtp_2
X_574_ clknet_2_1__leaf_clk _062_ _014_ VGND VGND VPWR VPWR counter1_o10_c sky130_fd_sc_hd__dfrtp_2
X_575_ clknet_2_1__leaf_clk _063_ _015_ VGND VGND VPWR VPWR counter1_o11_c sky130_fd_sc_hd__dfrtp_1
X_576_ clknet_2_0__leaf_clk _064_ _016_ VGND VGND VPWR VPWR counter2_o0_c sky130_fd_sc_hd__dfrtp_2
X_577_ clknet_2_2__leaf_clk _065_ _017_ VGND VGND VPWR VPWR counter2_o1_c sky130_fd_sc_hd__dfrtp_4
X_578_ clknet_2_0__leaf_clk _066_ _018_ VGND VGND VPWR VPWR counter2_o2_c sky130_fd_sc_hd__dfrtp_2
X_579_ clknet_2_2__leaf_clk _067_ _019_ VGND VGND VPWR VPWR counter2_o3_c sky130_fd_sc_hd__dfrtp_1
X_580_ clknet_2_2__leaf_clk _068_ _020_ VGND VGND VPWR VPWR counter2_o4_c sky130_fd_sc_hd__dfrtp_1
X_581_ clknet_2_2__leaf_clk _069_ _021_ VGND VGND VPWR VPWR counter2_o5_c sky130_fd_sc_hd__dfrtp_1
X_582_ clknet_2_2__leaf_clk _070_ _022_ VGND VGND VPWR VPWR counter2_o6_c sky130_fd_sc_hd__dfrtp_2
X_583_ clknet_2_2__leaf_clk _071_ _023_ VGND VGND VPWR VPWR counter2_o7_c sky130_fd_sc_hd__dfrtp_2
X_584_ clknet_2_3__leaf_clk _072_ _024_ VGND VGND VPWR VPWR pulse__counter_o0_c
+ sky130_fd_sc_hd__dfrtp_1
X_585_ clknet_2_1__leaf_clk _073_ _025_ VGND VGND VPWR VPWR pulse__counter_o1_c
+ sky130_fd_sc_hd__dfrtp_1
X_586_ clknet_2_1__leaf_clk _074_ _026_ VGND VGND VPWR VPWR pulse__counter_o2_c
+ sky130_fd_sc_hd__dfrtp_1
X_587_ clknet_2_1__leaf_clk _075_ _027_ VGND VGND VPWR VPWR pulse__counter_o3_c
+ sky130_fd_sc_hd__dfrtp_1
X_588_ clknet_2_3__leaf_clk _076_ _028_ VGND VGND VPWR VPWR pulse__counter_o4_c
+ sky130_fd_sc_hd__dfrtp_1
X_589_ clknet_2_3__leaf_clk _077_ _029_ VGND VGND VPWR VPWR pulse__counter_o5_c
+ sky130_fd_sc_hd__dfrtp_1
X_590_ clknet_2_3__leaf_clk _078_ _030_ VGND VGND VPWR VPWR pulse__counter_o6_c
+ sky130_fd_sc_hd__dfrtp_2
X_591_ clknet_2_3__leaf_clk _079_ _031_ VGND VGND VPWR VPWR pulse__counter_o7_c
+ sky130_fd_sc_hd__dfrtp_1
X_592_ clknet_2_3__leaf_clk _080_ _032_ VGND VGND VPWR VPWR pulse__counter_o8_c
+ sky130_fd_sc_hd__dfrtp_1
X_593_ clknet_2_2__leaf_clk _081_ _033_ VGND VGND VPWR VPWR pulse__counter_o9_c
+ sky130_fd_sc_hd__dfrtp_1
X_594_ clknet_2_2__leaf_clk _082_ _034_ VGND VGND VPWR VPWR pulse__counter_o10_c
+ sky130_fd_sc_hd__dfrtp_1
X_595_ clknet_2_3__leaf_clk _083_ _035_ VGND VGND VPWR VPWR pulse__counter_o11_c
+ sky130_fd_sc_hd__dfrtp_1
Xclkbuf_0_clk clk VGND VGND VPWR VPWR clknet_0_clk sky130_fd_sc_hd__clkbuf_16
Xclkbuf_2_0__f_clk clknet_0_clk VGND VGND VPWR VPWR clknet_2_0__leaf_clk sky130_fd_sc_hd__clkbuf_16
Xclkbuf_2_1__f_clk clknet_0_clk VGND VGND VPWR VPWR clknet_2_1__leaf_clk sky130_fd_sc_hd__clkbuf_16
Xclkbuf_2_2__f_clk clknet_0_clk VGND VGND VPWR VPWR clknet_2_2__leaf_clk sky130_fd_sc_hd__clkbuf_16
Xclkbuf_2_3__f_clk clknet_0_clk VGND VGND VPWR VPWR clknet_2_3__leaf_clk sky130_fd_sc_hd__clkbuf_16
Xhold1 net23 VGND VGND VPWR VPWR net38 sky130_fd_sc_hd__dlygate4sd3_1
Xhold10 pulse__counter_o2_c VGND VGND VPWR VPWR net47 sky130_fd_sc_hd__dlygate4sd3_1
Xhold11 net30 VGND VGND VPWR VPWR net48 sky130_fd_sc_hd__dlygate4sd3_1
Xhold12 pulse__counter_o7_c VGND VGND VPWR VPWR net49 sky130_fd_sc_hd__dlygate4sd3_1
Xhold13 net29 VGND VGND VPWR VPWR net50 sky130_fd_sc_hd__dlygate4sd3_1
Xhold14 net32 VGND VGND VPWR VPWR net51 sky130_fd_sc_hd__dlygate4sd3_1
Xhold15 pulse__counter_o10_c VGND VGND VPWR VPWR net52 sky130_fd_sc_hd__dlygate4sd3_1
Xhold16 net28 VGND VGND VPWR VPWR net53 sky130_fd_sc_hd__dlygate4sd3_1
Xhold17 pulse__counter_o9_c VGND VGND VPWR VPWR net54 sky130_fd_sc_hd__dlygate4sd3_1
Xhold18 net25 VGND VGND VPWR VPWR net55 sky130_fd_sc_hd__dlygate4sd3_1
Xhold19 _270_ VGND VGND VPWR VPWR net56 sky130_fd_sc_hd__dlygate4sd3_1
Xhold2 pulse__counter_o11_c VGND VGND VPWR VPWR net39 sky130_fd_sc_hd__dlygate4sd3_1
Xhold20 net26 VGND VGND VPWR VPWR net57 sky130_fd_sc_hd__dlygate4sd3_1
Xhold21 _271_ VGND VGND VPWR VPWR net58 sky130_fd_sc_hd__dlygate4sd3_1
Xhold22 pulse__counter_o1_c VGND VGND VPWR VPWR net59 sky130_fd_sc_hd__dlygate4sd3_1
Xhold23 net27 VGND VGND VPWR VPWR net60 sky130_fd_sc_hd__dlygate4sd3_1
Xhold24 pulse__counter_o0_c VGND VGND VPWR VPWR net61 sky130_fd_sc_hd__dlygate4sd3_1
Xhold25 _100_ VGND VGND VPWR VPWR net62 sky130_fd_sc_hd__dlygate4sd3_1
Xhold26 net24 VGND VGND VPWR VPWR net63 sky130_fd_sc_hd__dlygate4sd3_1
Xhold27 counter1_o11_c VGND VGND VPWR VPWR net64 sky130_fd_sc_hd__dlygate4sd3_1
Xhold28 counter1_o1_c VGND VGND VPWR VPWR net65 sky130_fd_sc_hd__dlygate4sd3_1
Xhold29 pulse__counter_o2_c VGND VGND VPWR VPWR net66 sky130_fd_sc_hd__dlygate4sd3_1
Xhold3 counter1_o0_c VGND VGND VPWR VPWR net40 sky130_fd_sc_hd__dlygate4sd3_1
Xhold30 pulse__counter_o9_c VGND VGND VPWR VPWR net67 sky130_fd_sc_hd__dlygate4sd3_1
Xhold4 pulse__counter_o4_c VGND VGND VPWR VPWR net41 sky130_fd_sc_hd__dlygate4sd3_1
Xhold5 pulse__counter_o3_c VGND VGND VPWR VPWR net42 sky130_fd_sc_hd__dlygate4sd3_1
Xhold6 net34 VGND VGND VPWR VPWR net43 sky130_fd_sc_hd__dlygate4sd3_1
Xhold7 net33 VGND VGND VPWR VPWR net44 sky130_fd_sc_hd__dlygate4sd3_1
Xhold8 net31 VGND VGND VPWR VPWR net45 sky130_fd_sc_hd__dlygate4sd3_1
Xhold9 net35 VGND VGND VPWR VPWR net46 sky130_fd_sc_hd__dlygate4sd3_1
Xinput1 c VGND VGND VPWR VPWR net1 sky130_fd_sc_hd__clkbuf_1
Xinput10 duty_cycle1[6] VGND VGND VPWR VPWR net10 sky130_fd_sc_hd__buf_1
Xinput11 duty_cycle1[7] VGND VGND VPWR VPWR net11 sky130_fd_sc_hd__buf_1
Xinput12 duty_cycle1[8] VGND VGND VPWR VPWR net12 sky130_fd_sc_hd__buf_1
Xinput13 duty_cycle1[9] VGND VGND VPWR VPWR net13 sky130_fd_sc_hd__buf_1
Xinput14 duty_cycle2[0] VGND VGND VPWR VPWR net14 sky130_fd_sc_hd__buf_1
Xinput15 duty_cycle2[1] VGND VGND VPWR VPWR net15 sky130_fd_sc_hd__buf_1
Xinput16 duty_cycle2[2] VGND VGND VPWR VPWR net16 sky130_fd_sc_hd__buf_1
Xinput17 duty_cycle2[3] VGND VGND VPWR VPWR net17 sky130_fd_sc_hd__buf_1
Xinput18 duty_cycle2[4] VGND VGND VPWR VPWR net18 sky130_fd_sc_hd__buf_1
Xinput19 duty_cycle2[5] VGND VGND VPWR VPWR net19 sky130_fd_sc_hd__buf_1
Xinput2 duty_cycle1[0] VGND VGND VPWR VPWR net2 sky130_fd_sc_hd__buf_1
Xinput20 duty_cycle2[6] VGND VGND VPWR VPWR net20 sky130_fd_sc_hd__clkbuf_1
Xinput21 duty_cycle2[7] VGND VGND VPWR VPWR net21 sky130_fd_sc_hd__buf_1
Xinput22 rst VGND VGND VPWR VPWR net22 sky130_fd_sc_hd__clkbuf_1
Xinput3 duty_cycle1[10] VGND VGND VPWR VPWR net3 sky130_fd_sc_hd__buf_1
Xinput4 duty_cycle1[11] VGND VGND VPWR VPWR net4 sky130_fd_sc_hd__buf_1
Xinput5 duty_cycle1[1] VGND VGND VPWR VPWR net5 sky130_fd_sc_hd__buf_1
Xinput6 duty_cycle1[2] VGND VGND VPWR VPWR net6 sky130_fd_sc_hd__buf_1
Xinput7 duty_cycle1[3] VGND VGND VPWR VPWR net7 sky130_fd_sc_hd__buf_1
Xinput8 duty_cycle1[4] VGND VGND VPWR VPWR net8 sky130_fd_sc_hd__buf_1
Xinput9 duty_cycle1[5] VGND VGND VPWR VPWR net9 sky130_fd_sc_hd__buf_1
Xoutput23 net23 VGND VGND VPWR VPWR enable sky130_fd_sc_hd__clkbuf_4
Xoutput24 net24 VGND VGND VPWR VPWR pulsecount_value[0] sky130_fd_sc_hd__clkbuf_4
Xoutput25 net25 VGND VGND VPWR VPWR pulsecount_value[10] sky130_fd_sc_hd__clkbuf_4
Xoutput26 net26 VGND VGND VPWR VPWR pulsecount_value[11] sky130_fd_sc_hd__clkbuf_4
Xoutput27 net27 VGND VGND VPWR VPWR pulsecount_value[1] sky130_fd_sc_hd__buf_2
Xoutput28 net28 VGND VGND VPWR VPWR pulsecount_value[2] sky130_fd_sc_hd__buf_2
Xoutput29 net29 VGND VGND VPWR VPWR pulsecount_value[3] sky130_fd_sc_hd__clkbuf_4
Xoutput30 net30 VGND VGND VPWR VPWR pulsecount_value[4] sky130_fd_sc_hd__buf_2
Xoutput31 net31 VGND VGND VPWR VPWR pulsecount_value[5] sky130_fd_sc_hd__buf_2
Xoutput32 net32 VGND VGND VPWR VPWR pulsecount_value[6] sky130_fd_sc_hd__buf_2
Xoutput33 net33 VGND VGND VPWR VPWR pulsecount_value[7] sky130_fd_sc_hd__buf_2
Xoutput34 net34 VGND VGND VPWR VPWR pulsecount_value[8] sky130_fd_sc_hd__buf_2
Xoutput35 net35 VGND VGND VPWR VPWR pulsecount_value[9] sky130_fd_sc_hd__buf_2
Xoutput36 net36 VGND VGND VPWR VPWR pwm_out1 sky130_fd_sc_hd__clkbuf_4
Xoutput37 net37 VGND VGND VPWR VPWR pwm_out2 sky130_fd_sc_hd__clkbuf_4
.ends

.GLOBAL GND
.end
